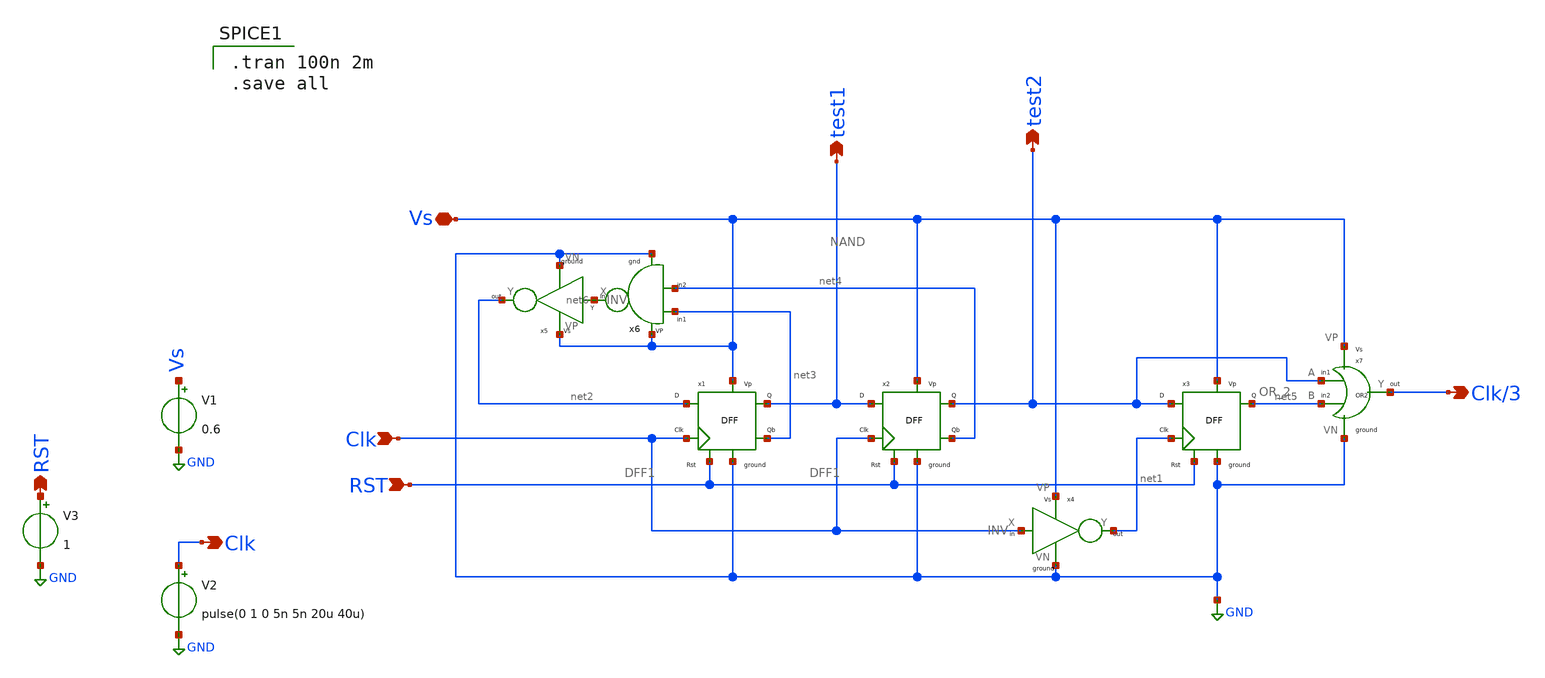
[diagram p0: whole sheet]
** sch_path: Blocks/Divide by 3 Circuit/Div3a.sch
**.subckt Div3a Clk/3 RST Clk Vs Clk RST test1 test2
*.opin Clk/3
*.ipin RST
*.ipin Clk
*.iopin Vs
*.opin Clk
*.opin RST
*.opin test1
*.opin test2
V1 Vs GND 0.6
x1 net2 Clk RST GND Vs test1 net3 DFF1
x2 test1 Clk RST GND Vs test2 net4 DFF1
x3 test2 net1 RST GND Vs net5 DFF
x7 net5 test2 Clk/3 Vs GND OR_2
V3 RST GND 1
x4 Clk net1 Vs GND INV
x5 net6 net2 Vs GND INV
x6 net4 net3 net6 Vs GND NAND
V2 Clk GND pulse(0 1 0 5n 5n 20u 40u)
**** begin user architecture code

** opencircuitdesign pdks install
.lib $::SKYWATER_MODELS/sky130.lib.spice tt



.tran 100n 2m
.save all

**** end user architecture code
**.ends

* expanding   symbol:  Pico_project/FlipFlops/DFF1.sym # of pins=7
** sym_path: component/FlipFlops/DFF1.sym
** sch_path: component/FlipFlops/DFF1.sch
.subckt DFF1 D Clk RST VN VP Q Qb
*.opin Q
*.iopin VN
*.iopin VP
*.ipin Clk
*.ipin D
*.ipin RST
*.opin Qb
x7 net2 net4 net3 VP VN NAND
x8 net3 Clk RST VP VN net2 NAND3
x6 Q net1 RST VP VN Qb NAND3
x4 net2 Clk net4 VP VN net1 NAND3
x5 net1 D RST VP VN net4 NAND3
x1 Qb net2 Q VP VN NAND
.ends


* expanding   symbol:  Pico_project/FlipFlops/DFF.sym # of pins=6
** sym_path: component/FlipFlops/DFF.sym
** sch_path: component/FlipFlops/DFF.sch
.subckt DFF D Clk RST VN VP Q
*.opin Q
*.iopin VN
*.iopin VP
*.ipin Clk
*.ipin D
*.ipin RST
x1 net2 net5 net4 VP VN NAND
x7 net4 Clk RST VP VN net2 NAND3
x3 Q net1 RST VP VN net3 NAND3
x4 net2 Clk net5 VP VN net1 NAND3
x5 net1 D RST VP VN net5 NAND3
x6 net3 net2 Q VP VN NAND
.ends


* expanding   symbol:  Pico_project/OR2/OR_2.sym # of pins=5
** sym_path: component/OR2/OR_2.sym
** sch_path: component/OR2/OR_2.sch
.subckt OR_2 B A Y VP VN
*.iopin VP
*.iopin VN
*.ipin A
*.ipin B
*.opin Y
XM1 net1 B VN VN sky130_fd_pr__nfet_01v8 L=0.15 W=0.42 nf=1 ad='int((nf+1)/2) * W/nf * 0.29' as='int((nf+2)/2) * W/nf * 0.29'
+ pd='2*int((nf+1)/2) * (W/nf + 0.29)' ps='2*int((nf+2)/2) * (W/nf + 0.29)' nrd='0.29 / W' nrs='0.29 / W'
+ sa=0 sb=0 sd=0 mult=1 m=1
XM2 net1 A VN VN sky130_fd_pr__nfet_01v8 L=0.15 W=0.42 nf=1 ad='int((nf+1)/2) * W/nf * 0.29' as='int((nf+2)/2) * W/nf * 0.29'
+ pd='2*int((nf+1)/2) * (W/nf + 0.29)' ps='2*int((nf+2)/2) * (W/nf + 0.29)' nrd='0.29 / W' nrs='0.29 / W'
+ sa=0 sb=0 sd=0 mult=1 m=1
XM3 net1 B net2 VP sky130_fd_pr__pfet_01v8 L=0.15 W=2.52 nf=1 ad='int((nf+1)/2) * W/nf * 0.29' as='int((nf+2)/2) * W/nf * 0.29'
+ pd='2*int((nf+1)/2) * (W/nf + 0.29)' ps='2*int((nf+2)/2) * (W/nf + 0.29)' nrd='0.29 / W' nrs='0.29 / W'
+ sa=0 sb=0 sd=0 mult=1 m=1
XM4 net2 A VP VP sky130_fd_pr__pfet_01v8 L=0.15 W=2.52 nf=1 ad='int((nf+1)/2) * W/nf * 0.29' as='int((nf+2)/2) * W/nf * 0.29'
+ pd='2*int((nf+1)/2) * (W/nf + 0.29)' ps='2*int((nf+2)/2) * (W/nf + 0.29)' nrd='0.29 / W' nrs='0.29 / W'
+ sa=0 sb=0 sd=0 mult=1 m=1
x1 net1 Y VP VN INV
.ends


* expanding   symbol:  Pico_project/INV/INV.sym # of pins=4
** sym_path: component/INV/INV.sym
** sch_path: component/INV/INV.sch
.subckt INV X Y VP VN
*.ipin X
*.opin Y
*.iopin VN
*.iopin VP
XM1 Y X VN VN sky130_fd_pr__nfet_01v8 L=0.15 W=0.42 nf=1 ad='int((nf+1)/2) * W/nf * 0.29' as='int((nf+2)/2) * W/nf * 0.29'
+ pd='2*int((nf+1)/2) * (W/nf + 0.29)' ps='2*int((nf+2)/2) * (W/nf + 0.29)' nrd='0.29 / W' nrs='0.29 / W'
+ sa=0 sb=0 sd=0 mult=1 m=1
XM2 Y X VP VP sky130_fd_pr__pfet_01v8 L=0.15 W=1.26 nf=1 ad='int((nf+1)/2) * W/nf * 0.29' as='int((nf+2)/2) * W/nf * 0.29'
+ pd='2*int((nf+1)/2) * (W/nf + 0.29)' ps='2*int((nf+2)/2) * (W/nf + 0.29)' nrd='0.29 / W' nrs='0.29 / W'
+ sa=0 sb=0 sd=0 mult=1 m=1
.ends


* expanding   symbol:  Pico_project/NAND2/NAND.sym # of pins=5
** sym_path: component/NAND2/NAND.sym
** sch_path: component/NAND2/NAND.sch
.subckt NAND B A Y VP VN
*.iopin VP
*.ipin A
*.ipin B
*.opin Y
*.iopin VN
XM1 Y A VP VP sky130_fd_pr__pfet_01v8 L=0.15 W=1.26 nf=1 ad='int((nf+1)/2) * W/nf * 0.29' as='int((nf+2)/2) * W/nf * 0.29'
+ pd='2*int((nf+1)/2) * (W/nf + 0.29)' ps='2*int((nf+2)/2) * (W/nf + 0.29)' nrd='0.29 / W' nrs='0.29 / W'
+ sa=0 sb=0 sd=0 mult=1 m=1
XM2 Y B VP VP sky130_fd_pr__pfet_01v8 L=0.15 W=1.26 nf=1 ad='int((nf+1)/2) * W/nf * 0.29' as='int((nf+2)/2) * W/nf * 0.29'
+ pd='2*int((nf+1)/2) * (W/nf + 0.29)' ps='2*int((nf+2)/2) * (W/nf + 0.29)' nrd='0.29 / W' nrs='0.29 / W'
+ sa=0 sb=0 sd=0 mult=1 m=1
XM3 Y A net1 net1 sky130_fd_pr__nfet_01v8 L=0.15 W=0.84 nf=1 ad='int((nf+1)/2) * W/nf * 0.29' as='int((nf+2)/2) * W/nf * 0.29'
+ pd='2*int((nf+1)/2) * (W/nf + 0.29)' ps='2*int((nf+2)/2) * (W/nf + 0.29)' nrd='0.29 / W' nrs='0.29 / W'
+ sa=0 sb=0 sd=0 mult=1 m=1
XM4 net1 B VN VN sky130_fd_pr__nfet_01v8 L=0.15 W=0.84 nf=1 ad='int((nf+1)/2) * W/nf * 0.29' as='int((nf+2)/2) * W/nf * 0.29'
+ pd='2*int((nf+1)/2) * (W/nf + 0.29)' ps='2*int((nf+2)/2) * (W/nf + 0.29)' nrd='0.29 / W' nrs='0.29 / W'
+ sa=0 sb=0 sd=0 mult=1 m=1
.ends


* expanding   symbol:  component/NAND3/NAND3.sym # of pins=6
** sym_path: component/NAND3/NAND3.sym
** sch_path: component/NAND3/NAND3.sch
.subckt NAND3 A B C VP VN Y
*.iopin VP
*.iopin VN
*.ipin A
*.ipin B
*.ipin C
*.opin Y
XM1 Y A net1 VN sky130_fd_pr__nfet_01v8 L=0.15 W=1.26 nf=1 ad='int((nf+1)/2) * W/nf * 0.29' as='int((nf+2)/2) * W/nf * 0.29'
+ pd='2*int((nf+1)/2) * (W/nf + 0.29)' ps='2*int((nf+2)/2) * (W/nf + 0.29)' nrd='0.29 / W' nrs='0.29 / W'
+ sa=0 sb=0 sd=0 mult=1 m=1
XM2 net1 B net2 VN sky130_fd_pr__nfet_01v8 L=0.15 W=1.26 nf=1 ad='int((nf+1)/2) * W/nf * 0.29' as='int((nf+2)/2) * W/nf * 0.29'
+ pd='2*int((nf+1)/2) * (W/nf + 0.29)' ps='2*int((nf+2)/2) * (W/nf + 0.29)' nrd='0.29 / W' nrs='0.29 / W'
+ sa=0 sb=0 sd=0 mult=1 m=1
XM3 net2 C VN VN sky130_fd_pr__nfet_01v8 L=0.15 W=1.26 nf=1 ad='int((nf+1)/2) * W/nf * 0.29' as='int((nf+2)/2) * W/nf * 0.29'
+ pd='2*int((nf+1)/2) * (W/nf + 0.29)' ps='2*int((nf+2)/2) * (W/nf + 0.29)' nrd='0.29 / W' nrs='0.29 / W'
+ sa=0 sb=0 sd=0 mult=1 m=1
XM4 Y A VP VP sky130_fd_pr__pfet_01v8 L=0.15 W=1.26 nf=1 ad='int((nf+1)/2) * W/nf * 0.29' as='int((nf+2)/2) * W/nf * 0.29'
+ pd='2*int((nf+1)/2) * (W/nf + 0.29)' ps='2*int((nf+2)/2) * (W/nf + 0.29)' nrd='0.29 / W' nrs='0.29 / W'
+ sa=0 sb=0 sd=0 mult=1 m=1
XM5 Y B VP VP sky130_fd_pr__pfet_01v8 L=0.15 W=1.26 nf=1 ad='int((nf+1)/2) * W/nf * 0.29' as='int((nf+2)/2) * W/nf * 0.29'
+ pd='2*int((nf+1)/2) * (W/nf + 0.29)' ps='2*int((nf+2)/2) * (W/nf + 0.29)' nrd='0.29 / W' nrs='0.29 / W'
+ sa=0 sb=0 sd=0 mult=1 m=1
XM6 Y C VP VP sky130_fd_pr__pfet_01v8 L=0.15 W=1.26 nf=1 ad='int((nf+1)/2) * W/nf * 0.29' as='int((nf+2)/2) * W/nf * 0.29'
+ pd='2*int((nf+1)/2) * (W/nf + 0.29)' ps='2*int((nf+2)/2) * (W/nf + 0.29)' nrd='0.29 / W' nrs='0.29 / W'
+ sa=0 sb=0 sd=0 mult=1 m=1
.ends

.GLOBAL GND
.end
